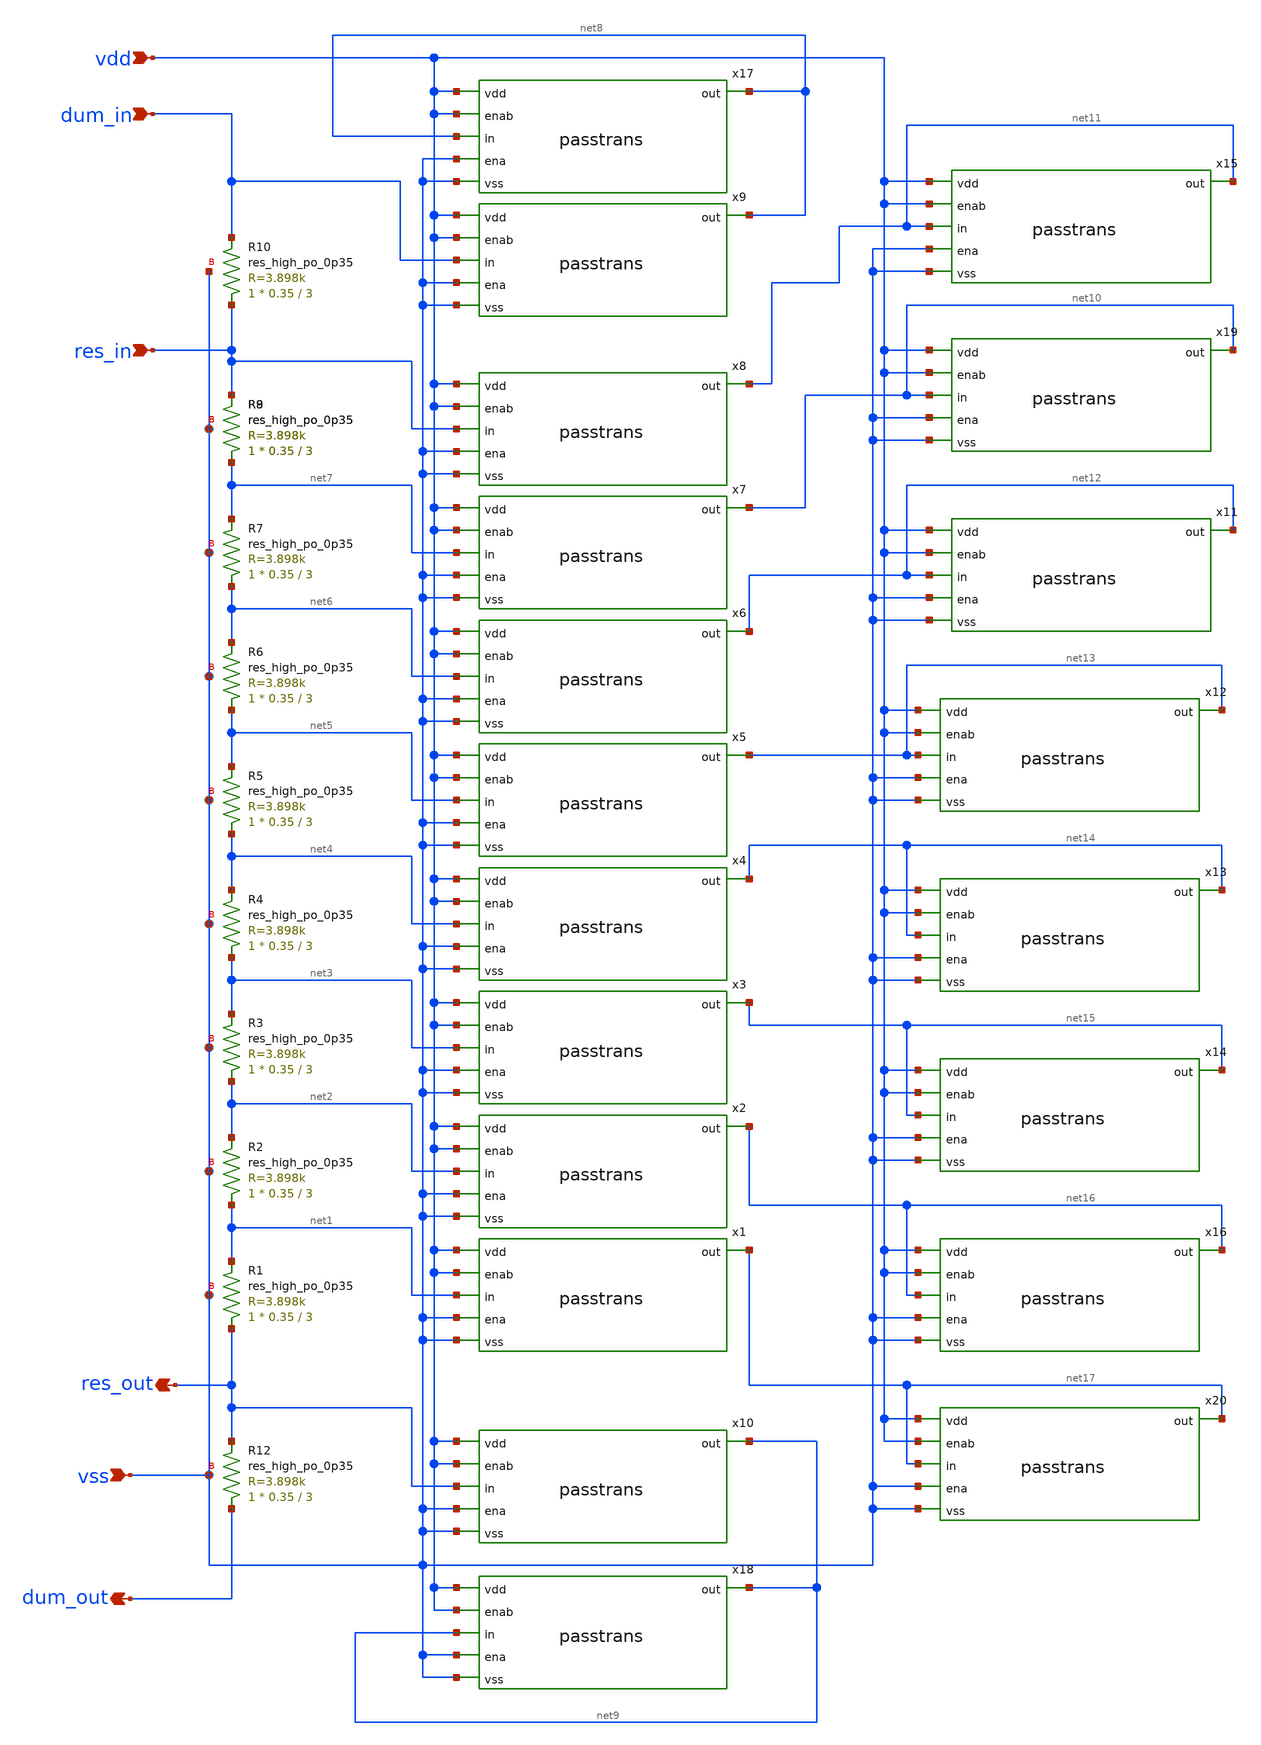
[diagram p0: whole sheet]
** sch_path: xschem/dac_column_dummy.sch
**.subckt dac_column_dummy res_in vss vdd dum_in res_out dum_out
*.ipin res_in
*.ipin vss
*.ipin vdd
*.ipin dum_in
*.opin res_out
*.opin dum_out
x1 vdd vdd net17 net1 vss vss passtrans
XR1 res_out net1 vss sky130_fd_pr__res_high_po_0p35 L=3 mult=1 m=1
x2 vdd vdd net16 net2 vss vss passtrans
x3 vdd vdd net15 net3 vss vss passtrans
x4 vdd vdd net14 net4 vss vss passtrans
x5 vdd vdd net13 net5 vss vss passtrans
x6 vdd vdd net12 net6 vss vss passtrans
x7 vdd vdd net10 net7 vss vss passtrans
x8 vdd vdd net11 res_in vss vss passtrans
x9 vdd vdd net8 dum_in vss vss passtrans
x10 vdd vdd net9 res_out vss vss passtrans
XR2 net1 net2 vss sky130_fd_pr__res_high_po_0p35 L=3 mult=1 m=1
XR3 net2 net3 vss sky130_fd_pr__res_high_po_0p35 L=3 mult=1 m=1
XR4 net3 net4 vss sky130_fd_pr__res_high_po_0p35 L=3 mult=1 m=1
XR5 net4 net5 vss sky130_fd_pr__res_high_po_0p35 L=3 mult=1 m=1
XR6 net5 net6 vss sky130_fd_pr__res_high_po_0p35 L=3 mult=1 m=1
XR7 net6 net7 vss sky130_fd_pr__res_high_po_0p35 L=3 mult=1 m=1
XR8 net7 res_in vss sky130_fd_pr__res_high_po_0p35 L=3 mult=1 m=1
XR9 net7 res_in vss sky130_fd_pr__res_high_po_0p35 L=3 mult=1 m=1
XR10 res_in dum_in vss sky130_fd_pr__res_high_po_0p35 L=3 mult=1 m=1
XR12 dum_out res_out vss sky130_fd_pr__res_high_po_0p35 L=3 mult=1 m=1
x11 vdd vdd net12 net12 vss vss passtrans
x12 vdd vdd net13 net13 vss vss passtrans
x13 vdd vdd net14 net14 vss vss passtrans
x14 vdd vdd net15 net15 vss vss passtrans
x15 vdd vdd net11 net11 vss vss passtrans
x16 vdd vdd net16 net16 vss vss passtrans
x17 vdd vdd net8 net8 vss vss passtrans
x18 vdd vdd net9 net9 vss vss passtrans
x19 vdd vdd net10 net10 vss vss passtrans
x20 vdd vdd net17 net17 vss vss passtrans
**.ends

* expanding   symbol:  passtrans.sym # of pins=6
** sym_path: xschem/passtrans.sym
** sch_path: xschem/passtrans.sch
.subckt passtrans vdd enab out in ena vss
*.ipin enab
*.ipin ena
*.ipin vss
*.ipin vdd
*.ipin in
*.opin out
XM1 in ena out vss sky130_fd_pr__nfet_g5v0d10v5 L=0.5 W=0.65 nf=1 ad='int((nf+1)/2) * W/nf * 0.29' as='int((nf+2)/2) * W/nf * 0.29'
+ pd='2*int((nf+1)/2) * (W/nf + 0.29)' ps='2*int((nf+2)/2) * (W/nf + 0.29)' nrd='0.29 / W' nrs='0.29 / W'
+ sa=0 sb=0 sd=0 mult=1 m=1
XM2 in enab out vdd sky130_fd_pr__pfet_g5v0d10v5 L=0.5 W=1 nf=1 ad='int((nf+1)/2) * W/nf * 0.29' as='int((nf+2)/2) * W/nf * 0.29'
+ pd='2*int((nf+1)/2) * (W/nf + 0.29)' ps='2*int((nf+2)/2) * (W/nf + 0.29)' nrd='0.29 / W' nrs='0.29 / W'
+ sa=0 sb=0 sd=0 mult=1 m=1
.ends

.end
